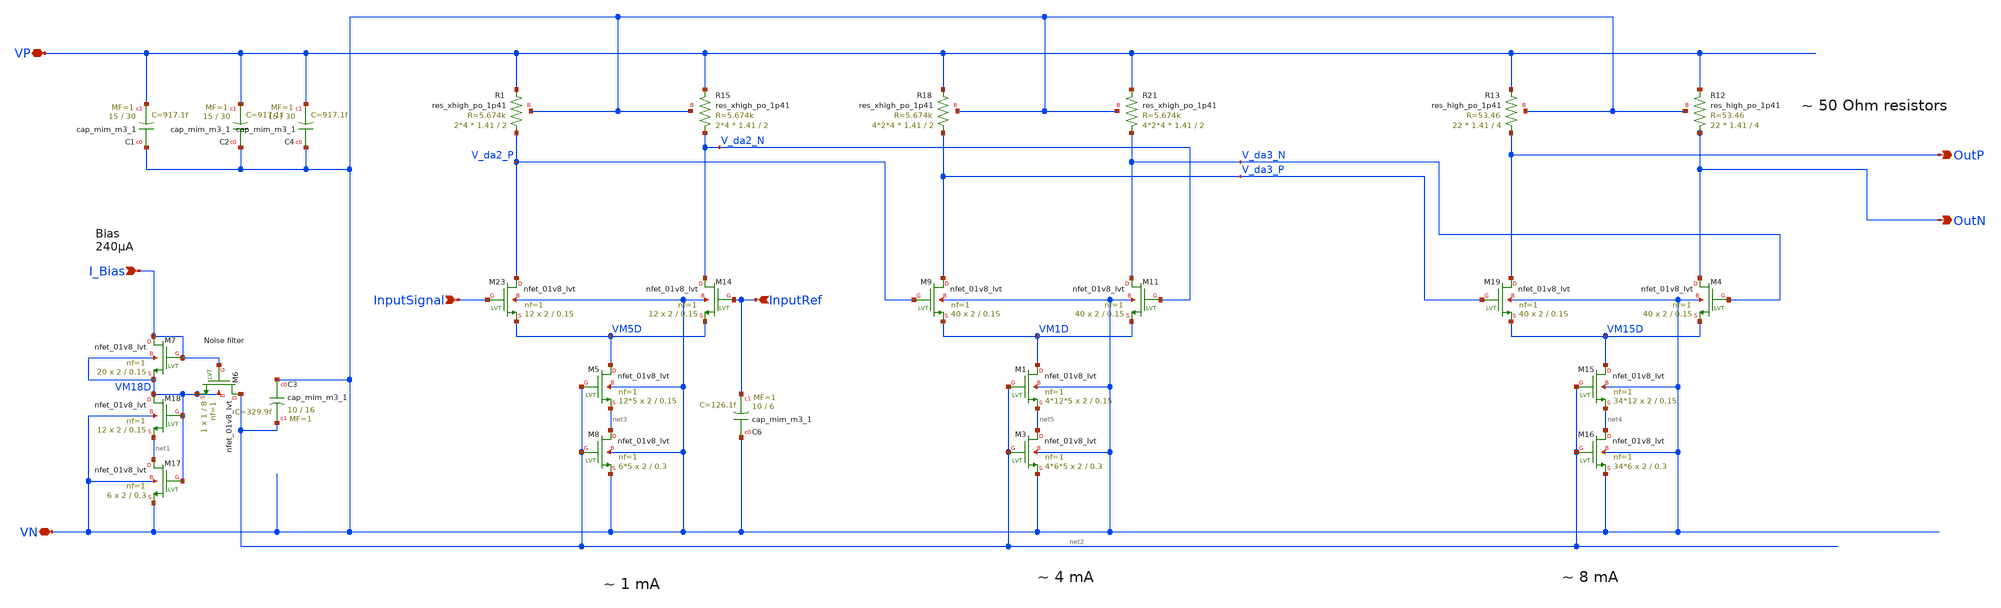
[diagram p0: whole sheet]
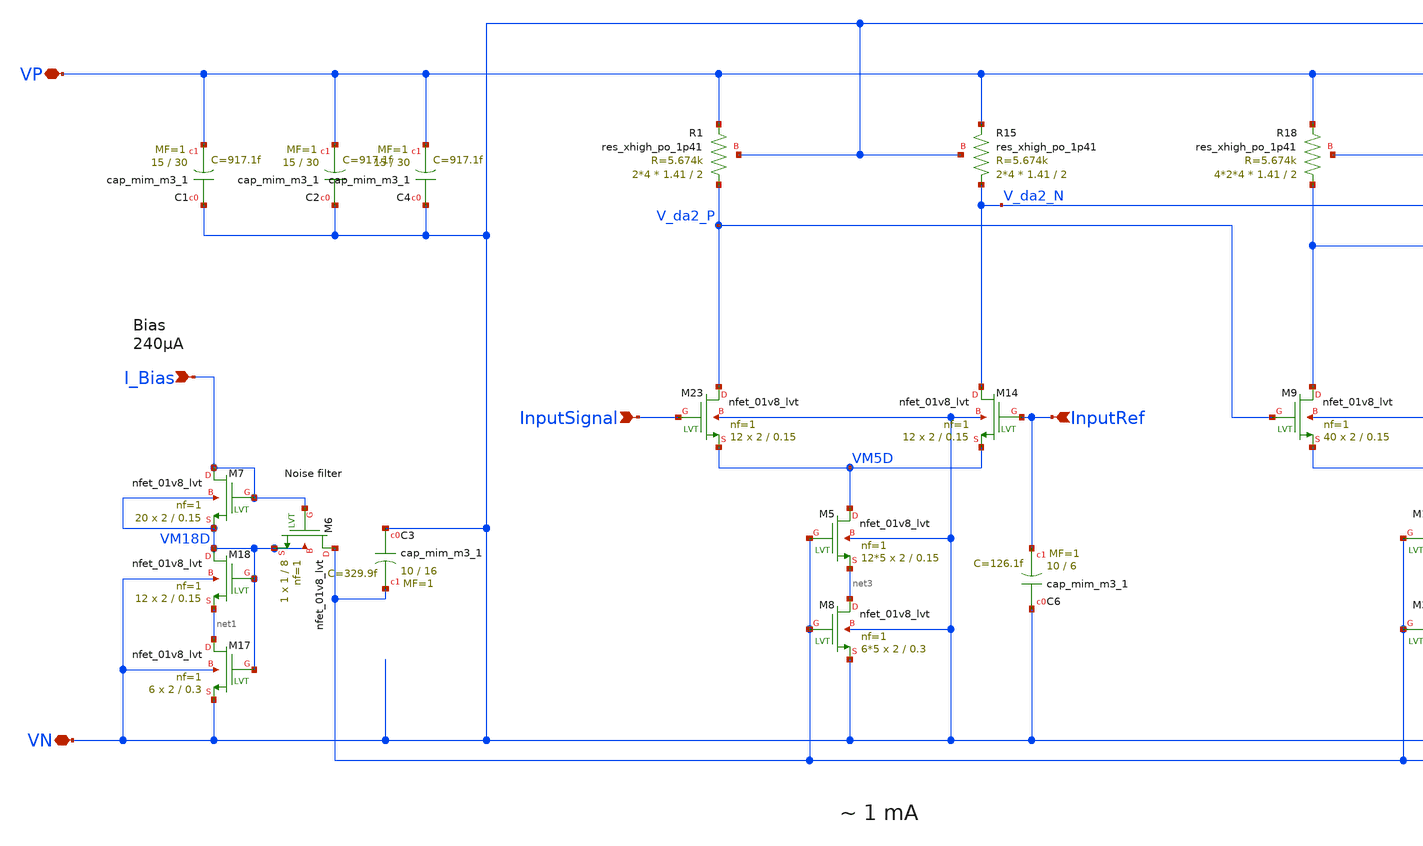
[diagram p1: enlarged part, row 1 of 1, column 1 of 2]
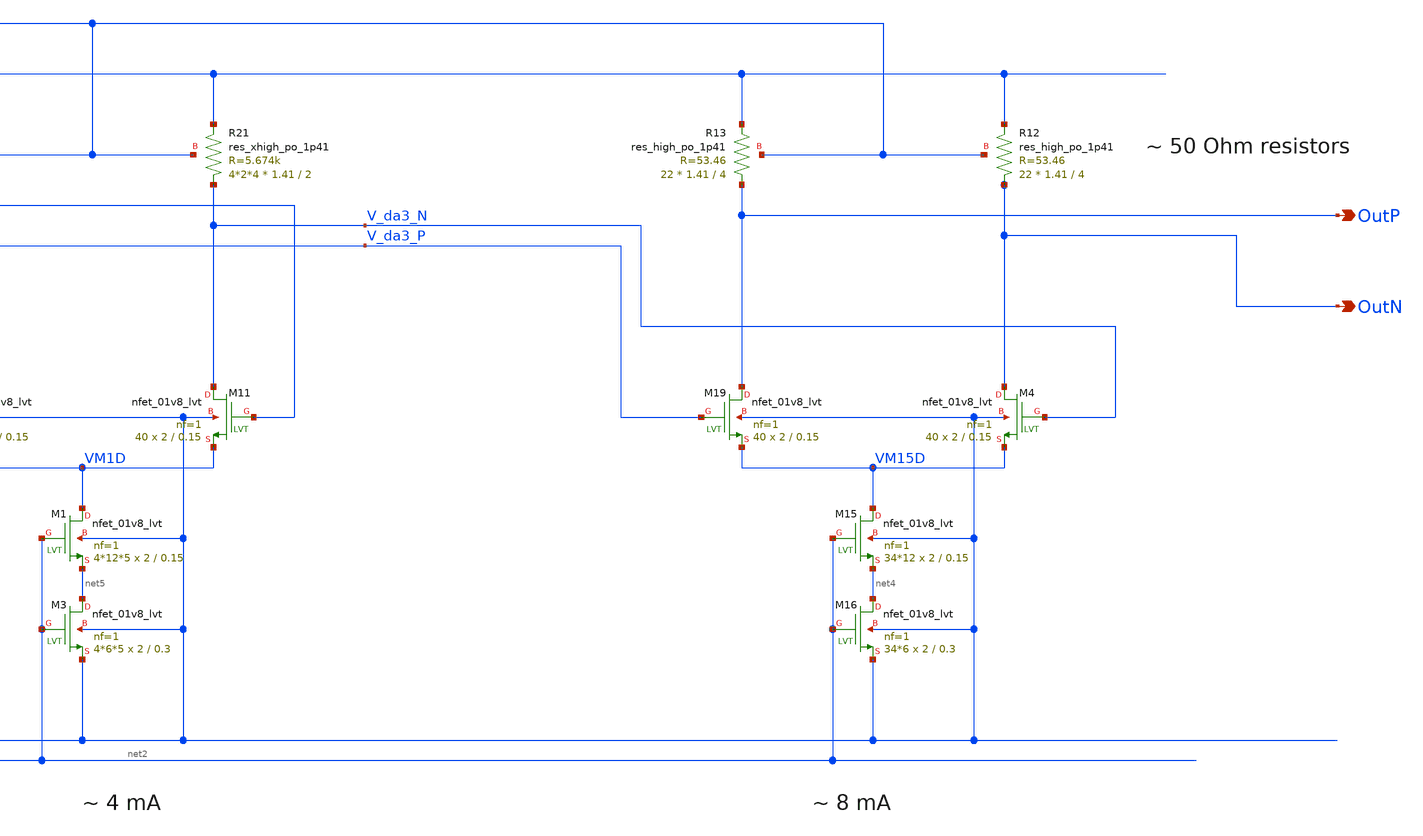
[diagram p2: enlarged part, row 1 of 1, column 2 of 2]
** sch_path: xschem/outdriver/outdriver_50ohm.sch
**.subckt outdriver_50ohm VN InputRef VP I_Bias InputSignal OutN OutP
*.iopin VN
*.ipin InputRef
*.iopin VP
*.ipin I_Bias
*.ipin InputSignal
*.opin OutN
*.opin OutP
XM17 net1 VM18D VN VN sky130_fd_pr__nfet_01v8_lvt L=0.3 W=2 nf=1 ad='int((nf+1)/2) * W/nf * 0.29' as='int((nf+2)/2) * W/nf * 0.29'
+ pd='2*int((nf+1)/2) * (W/nf + 0.29)' ps='2*int((nf+2)/2) * (W/nf + 0.29)' nrd='0.29 / W' nrs='0.29 / W'
+ sa=0 sb=0 sd=0 mult=6 m=6
XM18 VM18D VM18D net1 VN sky130_fd_pr__nfet_01v8_lvt L=0.15 W=2 nf=1 ad='int((nf+1)/2) * W/nf * 0.29'
+ as='int((nf+2)/2) * W/nf * 0.29' pd='2*int((nf+1)/2) * (W/nf + 0.29)' ps='2*int((nf+2)/2) * (W/nf + 0.29)'
+ nrd='0.29 / W' nrs='0.29 / W' sa=0 sb=0 sd=0 mult=12 m=12
XM7 I_Bias I_Bias VM18D VM18D sky130_fd_pr__nfet_01v8_lvt L=0.15 W=2 nf=1 ad='int((nf+1)/2) * W/nf * 0.29'
+ as='int((nf+2)/2) * W/nf * 0.29' pd='2*int((nf+1)/2) * (W/nf + 0.29)' ps='2*int((nf+2)/2) * (W/nf + 0.29)'
+ nrd='0.29 / W' nrs='0.29 / W' sa=0 sb=0 sd=0 mult=20 m=20
XM5 VM5D net2 net3 VN sky130_fd_pr__nfet_01v8_lvt L=0.15 W=2 nf=1 ad='int((nf+1)/2) * W/nf * 0.29' as='int((nf+2)/2) * W/nf * 0.29'
+ pd='2*int((nf+1)/2) * (W/nf + 0.29)' ps='2*int((nf+2)/2) * (W/nf + 0.29)' nrd='0.29 / W' nrs='0.29 / W'
+ sa=0 sb=0 sd=0 mult=12*5 m=12*5
XM8 net3 net2 VN VN sky130_fd_pr__nfet_01v8_lvt L=0.3 W=2 nf=1 ad='int((nf+1)/2) * W/nf * 0.29' as='int((nf+2)/2) * W/nf * 0.29'
+ pd='2*int((nf+1)/2) * (W/nf + 0.29)' ps='2*int((nf+2)/2) * (W/nf + 0.29)' nrd='0.29 / W' nrs='0.29 / W'
+ sa=0 sb=0 sd=0 mult=6*5 m=6*5
XM6 net2 I_Bias VM18D VM18D sky130_fd_pr__nfet_01v8_lvt L=8 W=1 nf=1 ad='int((nf+1)/2) * W/nf * 0.29'
+ as='int((nf+2)/2) * W/nf * 0.29' pd='2*int((nf+1)/2) * (W/nf + 0.29)' ps='2*int((nf+2)/2) * (W/nf + 0.29)'
+ nrd='0.29 / W' nrs='0.29 / W' sa=0 sb=0 sd=0 mult=1 m=1
XC1 VN VP sky130_fd_pr__cap_mim_m3_1 W=15 L=30 MF=1 m=1
XM15 VM15D net2 net4 VN sky130_fd_pr__nfet_01v8_lvt L=0.15 W=2 nf=1 ad='int((nf+1)/2) * W/nf * 0.29'
+ as='int((nf+2)/2) * W/nf * 0.29' pd='2*int((nf+1)/2) * (W/nf + 0.29)' ps='2*int((nf+2)/2) * (W/nf + 0.29)'
+ nrd='0.29 / W' nrs='0.29 / W' sa=0 sb=0 sd=0 mult=34*12 m=34*12
XM16 net4 net2 VN VN sky130_fd_pr__nfet_01v8_lvt L=0.3 W=2 nf=1 ad='int((nf+1)/2) * W/nf * 0.29' as='int((nf+2)/2) * W/nf * 0.29'
+ pd='2*int((nf+1)/2) * (W/nf + 0.29)' ps='2*int((nf+2)/2) * (W/nf + 0.29)' nrd='0.29 / W' nrs='0.29 / W'
+ sa=0 sb=0 sd=0 mult=34*6 m=34*6
XM4 OutN V_da3_N VM15D VN sky130_fd_pr__nfet_01v8_lvt L=0.15 W=2 nf=1 ad='int((nf+1)/2) * W/nf * 0.29'
+ as='int((nf+2)/2) * W/nf * 0.29' pd='2*int((nf+1)/2) * (W/nf + 0.29)' ps='2*int((nf+2)/2) * (W/nf + 0.29)'
+ nrd='0.29 / W' nrs='0.29 / W' sa=0 sb=0 sd=0 mult=40 m=40
XM23 V_da2_P InputSignal VM5D VN sky130_fd_pr__nfet_01v8_lvt L=0.15 W=2 nf=1 ad='int((nf+1)/2) * W/nf * 0.29'
+ as='int((nf+2)/2) * W/nf * 0.29' pd='2*int((nf+1)/2) * (W/nf + 0.29)' ps='2*int((nf+2)/2) * (W/nf + 0.29)'
+ nrd='0.29 / W' nrs='0.29 / W' sa=0 sb=0 sd=0 mult=12 m=12
XM19 OutP V_da3_P VM15D VN sky130_fd_pr__nfet_01v8_lvt L=0.15 W=2 nf=1 ad='int((nf+1)/2) * W/nf * 0.29'
+ as='int((nf+2)/2) * W/nf * 0.29' pd='2*int((nf+1)/2) * (W/nf + 0.29)' ps='2*int((nf+2)/2) * (W/nf + 0.29)'
+ nrd='0.29 / W' nrs='0.29 / W' sa=0 sb=0 sd=0 mult=40 m=40
XM14 V_da2_N InputRef VM5D VN sky130_fd_pr__nfet_01v8_lvt L=0.15 W=2 nf=1 ad='int((nf+1)/2) * W/nf * 0.29'
+ as='int((nf+2)/2) * W/nf * 0.29' pd='2*int((nf+1)/2) * (W/nf + 0.29)' ps='2*int((nf+2)/2) * (W/nf + 0.29)'
+ nrd='0.29 / W' nrs='0.29 / W' sa=0 sb=0 sd=0 mult=12 m=12
XR12 OutN VP VN sky130_fd_pr__res_high_po_1p41 L=4 mult=22 m=22
XR13 OutP VP VN sky130_fd_pr__res_high_po_1p41 L=4 mult=22 m=22
XM1 VM1D net2 net5 VN sky130_fd_pr__nfet_01v8_lvt L=0.15 W=2 nf=1 ad='int((nf+1)/2) * W/nf * 0.29' as='int((nf+2)/2) * W/nf * 0.29'
+ pd='2*int((nf+1)/2) * (W/nf + 0.29)' ps='2*int((nf+2)/2) * (W/nf + 0.29)' nrd='0.29 / W' nrs='0.29 / W'
+ sa=0 sb=0 sd=0 mult=4*12*5 m=4*12*5
XM3 net5 net2 VN VN sky130_fd_pr__nfet_01v8_lvt L=0.3 W=2 nf=1 ad='int((nf+1)/2) * W/nf * 0.29' as='int((nf+2)/2) * W/nf * 0.29'
+ pd='2*int((nf+1)/2) * (W/nf + 0.29)' ps='2*int((nf+2)/2) * (W/nf + 0.29)' nrd='0.29 / W' nrs='0.29 / W'
+ sa=0 sb=0 sd=0 mult=4*6*5 m=4*6*5
XM9 V_da3_P V_da2_P VM1D VN sky130_fd_pr__nfet_01v8_lvt L=0.15 W=2 nf=1 ad='int((nf+1)/2) * W/nf * 0.29'
+ as='int((nf+2)/2) * W/nf * 0.29' pd='2*int((nf+1)/2) * (W/nf + 0.29)' ps='2*int((nf+2)/2) * (W/nf + 0.29)'
+ nrd='0.29 / W' nrs='0.29 / W' sa=0 sb=0 sd=0 mult=40 m=40
XM11 V_da3_N V_da2_N VM1D VN sky130_fd_pr__nfet_01v8_lvt L=0.15 W=2 nf=1 ad='int((nf+1)/2) * W/nf * 0.29'
+ as='int((nf+2)/2) * W/nf * 0.29' pd='2*int((nf+1)/2) * (W/nf + 0.29)' ps='2*int((nf+2)/2) * (W/nf + 0.29)'
+ nrd='0.29 / W' nrs='0.29 / W' sa=0 sb=0 sd=0 mult=40 m=40
XR1 V_da2_P VP VN sky130_fd_pr__res_xhigh_po_1p41 L=2 mult=2*4 m=2*4
XR15 V_da2_N VP VN sky130_fd_pr__res_xhigh_po_1p41 L=2 mult=2*4 m=2*4
XR18 V_da3_P VP VN sky130_fd_pr__res_xhigh_po_1p41 L=2 mult=4*2*4 m=4*2*4
XR21 V_da3_N VP VN sky130_fd_pr__res_xhigh_po_1p41 L=2 mult=4*2*4 m=4*2*4
XC6 VN InputRef sky130_fd_pr__cap_mim_m3_1 W=10 L=6 MF=1 m=1
XC2 VN VP sky130_fd_pr__cap_mim_m3_1 W=15 L=30 MF=1 m=1
XC4 VN VP sky130_fd_pr__cap_mim_m3_1 W=15 L=30 MF=1 m=1
XC3 VN net2 sky130_fd_pr__cap_mim_m3_1 W=10 L=16 MF=1 m=1
**.ends
.end
